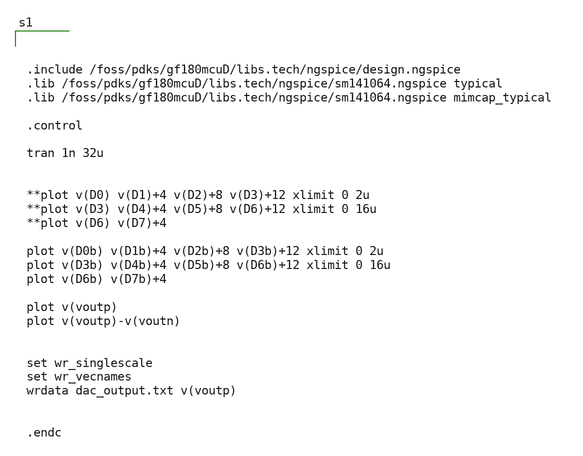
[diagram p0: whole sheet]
** sch_path: analog/dac/untitled-2.sch
**.subckt untitled-2
**** begin user architecture code



.include /foss/pdks/gf180mcuD/libs.tech/ngspice/design.ngspice
.lib /foss/pdks/gf180mcuD/libs.tech/ngspice/sm141064.ngspice typical
.lib /foss/pdks/gf180mcuD/libs.tech/ngspice/sm141064.ngspice mimcap_typical

.control

tran 1n 32u


**plot v(D0) v(D1)+4 v(D2)+8 v(D3)+12 xlimit 0 2u
**plot v(D3) v(D4)+4 v(D5)+8 v(D6)+12 xlimit 0 16u
**plot v(D6) v(D7)+4

plot v(D0b) v(D1b)+4 v(D2b)+8 v(D3b)+12 xlimit 0 2u
plot v(D3b) v(D4b)+4 v(D5b)+8 v(D6b)+12 xlimit 0 16u
plot v(D6b) v(D7b)+4

plot v(voutp)
plot v(voutp)-v(voutn)


set wr_singlescale
set wr_vecnames
wrdata dac_output.txt v(voutp)


.endc



**** end user architecture code
**.ends
.end
